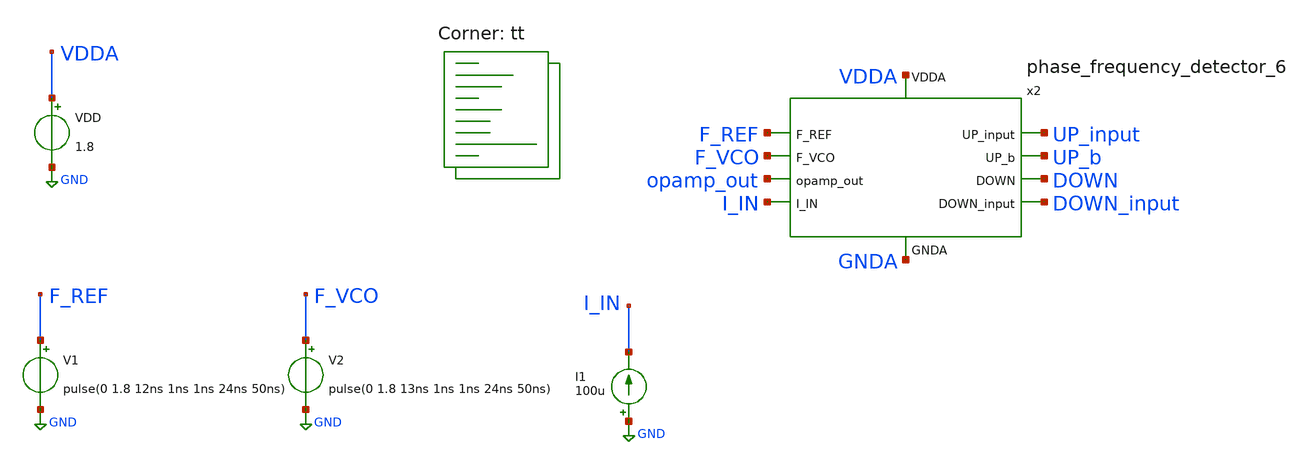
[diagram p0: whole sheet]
** sch_path: projects/pll/pfd/xschem_ngspice/tb_phase_frequency_detector_3.sch
**.subckt tb_phase_frequency_detector_3
V1 F_REF GND pulse(0 1.8 12ns 1ns 1ns 24ns 50ns)
V2 F_VCO GND pulse(0 1.8 13ns 1ns 1ns 24ns 50ns)
VDD VDDA GND 1.8
x2 UP_input VDDA GNDA UP_b F_REF DOWN F_VCO DOWN_input opamp_out I_IN phase_frequency_detector_6
I1 GND I_IN 100u
**** begin user architecture code
.lib $::SKYWATER_MODELS/sky130.lib.spice tt



.option wnflag=1
.option method=gear trtol=1

.save v(x1.reset)
.save v(x1.qb_b)
.save v(x1.qa_b)
.save v(x1.f_b)
.save v(x1.f)
.save v(x1.e_b)
.save v(x1.e)
.save v(x1.before_reset)
.save v(qb)
.save v(qa)
.save v(f_vco)
.save v(f_ref)
.save v(f_vco)

.control

  tran 1ns 1us
  remzerovec
  write tb_phase_frequency_detector_3.raw
  set appendwrite

.endc



**** end user architecture code
**.ends

* expanding   symbol:  phase_frequency_detector_6.sym # of pins=10
** sym_path: projects/pll/pfd/xschem_ngspice/phase_frequency_detector_6.sym
** sch_path: projects/pll/pfd/xschem_ngspice/phase_frequency_detector_6.sch
.subckt phase_frequency_detector_6 UP_input VDDA GNDA UP_b F_REF DOWN F_VCO DOWN_input opamp_out
+ I_IN
*.ipin F_REF
*.ipin F_VCO
*.ipin VDDA
*.ipin GNDA
*.opin UP_input
*.opin DOWN_input
*.opin UP_b
*.opin DOWN
*.ipin opamp_out
*.ipin I_IN
XM1 DOWN_b GNDA DOWN_PFD_b VDDA sky130_fd_pr__pfet_01v8 L=0.15 W=2 nf=2 ad='int((nf+1)/2) * W/nf * 0.29'
+ as='int((nf+2)/2) * W/nf * 0.29' pd='2*int((nf+1)/2) * (W/nf + 0.29)' ps='2*int((nf+2)/2) * (W/nf + 0.29)'
+ nrd='0.29 / W' nrs='0.29 / W' sa=0 sb=0 sd=0 mult=1 m=1
XM2 DOWN_b VDDA DOWN_PFD_b GNDA sky130_fd_pr__nfet_01v8 L=0.15 W=1 nf=1 ad='int((nf+1)/2) * W/nf * 0.29'
+ as='int((nf+2)/2) * W/nf * 0.29' pd='2*int((nf+1)/2) * (W/nf + 0.29)' ps='2*int((nf+2)/2) * (W/nf + 0.29)'
+ nrd='0.29 / W' nrs='0.29 / W' sa=0 sb=0 sd=0 mult=1 m=1
XM3 DOWN_PFD_b QB VDDA VDDA sky130_fd_pr__pfet_01v8 L=0.15 W=2 nf=2 ad='int((nf+1)/2) * W/nf * 0.29'
+ as='int((nf+2)/2) * W/nf * 0.29' pd='2*int((nf+1)/2) * (W/nf + 0.29)' ps='2*int((nf+2)/2) * (W/nf + 0.29)'
+ nrd='0.29 / W' nrs='0.29 / W' sa=0 sb=0 sd=0 mult=1 m=1
XM4 GNDA QB DOWN_PFD_b GNDA sky130_fd_pr__nfet_01v8 L=0.15 W=1 nf=1 ad='int((nf+1)/2) * W/nf * 0.29'
+ as='int((nf+2)/2) * W/nf * 0.29' pd='2*int((nf+1)/2) * (W/nf + 0.29)' ps='2*int((nf+2)/2) * (W/nf + 0.29)'
+ nrd='0.29 / W' nrs='0.29 / W' sa=0 sb=0 sd=0 mult=1 m=1
XM5 UP_PFD_b QA VDDA VDDA sky130_fd_pr__pfet_01v8 L=0.15 W=2 nf=2 ad='int((nf+1)/2) * W/nf * 0.29' as='int((nf+2)/2) * W/nf * 0.29'
+ pd='2*int((nf+1)/2) * (W/nf + 0.29)' ps='2*int((nf+2)/2) * (W/nf + 0.29)' nrd='0.29 / W' nrs='0.29 / W'
+ sa=0 sb=0 sd=0 mult=1 m=1
XM6 GNDA QA UP_PFD_b GNDA sky130_fd_pr__nfet_01v8 L=0.15 W=1 nf=1 ad='int((nf+1)/2) * W/nf * 0.29' as='int((nf+2)/2) * W/nf * 0.29'
+ pd='2*int((nf+1)/2) * (W/nf + 0.29)' ps='2*int((nf+2)/2) * (W/nf + 0.29)' nrd='0.29 / W' nrs='0.29 / W'
+ sa=0 sb=0 sd=0 mult=1 m=1
XM7 UP UP_PFD_b VDDA VDDA sky130_fd_pr__pfet_01v8 L=0.15 W=2 nf=2 ad='int((nf+1)/2) * W/nf * 0.29' as='int((nf+2)/2) * W/nf * 0.29'
+ pd='2*int((nf+1)/2) * (W/nf + 0.29)' ps='2*int((nf+2)/2) * (W/nf + 0.29)' nrd='0.29 / W' nrs='0.29 / W'
+ sa=0 sb=0 sd=0 mult=1 m=1
XM8 GNDA UP_PFD_b UP GNDA sky130_fd_pr__nfet_01v8 L=0.15 W=1 nf=1 ad='int((nf+1)/2) * W/nf * 0.29' as='int((nf+2)/2) * W/nf * 0.29'
+ pd='2*int((nf+1)/2) * (W/nf + 0.29)' ps='2*int((nf+2)/2) * (W/nf + 0.29)' nrd='0.29 / W' nrs='0.29 / W'
+ sa=0 sb=0 sd=0 mult=1 m=1
XM9 UP_input UP_b opamp_out VDDA sky130_fd_pr__pfet_01v8 L=0.15 W=2 nf=2 ad='int((nf+1)/2) * W/nf * 0.29'
+ as='int((nf+2)/2) * W/nf * 0.29' pd='2*int((nf+1)/2) * (W/nf + 0.29)' ps='2*int((nf+2)/2) * (W/nf + 0.29)'
+ nrd='0.29 / W' nrs='0.29 / W' sa=0 sb=0 sd=0 mult=1 m=1
XM18 UP_input UP VDDA VDDA sky130_fd_pr__pfet_01v8 L=0.15 W=2 nf=2 ad='int((nf+1)/2) * W/nf * 0.29' as='int((nf+2)/2) * W/nf * 0.29'
+ pd='2*int((nf+1)/2) * (W/nf + 0.29)' ps='2*int((nf+2)/2) * (W/nf + 0.29)' nrd='0.29 / W' nrs='0.29 / W'
+ sa=0 sb=0 sd=0 mult=1 m=1
XM19 DOWN_input DOWN I_IN GNDA sky130_fd_pr__nfet_01v8 L=0.15 W=1 nf=1 ad='int((nf+1)/2) * W/nf * 0.29'
+ as='int((nf+2)/2) * W/nf * 0.29' pd='2*int((nf+1)/2) * (W/nf + 0.29)' ps='2*int((nf+2)/2) * (W/nf + 0.29)'
+ nrd='0.29 / W' nrs='0.29 / W' sa=0 sb=0 sd=0 mult=1 m=1
XM20 DOWN_input DOWN_b GNDA GNDA sky130_fd_pr__nfet_01v8 L=0.15 W=1 nf=1 ad='int((nf+1)/2) * W/nf * 0.29'
+ as='int((nf+2)/2) * W/nf * 0.29' pd='2*int((nf+1)/2) * (W/nf + 0.29)' ps='2*int((nf+2)/2) * (W/nf + 0.29)'
+ nrd='0.29 / W' nrs='0.29 / W' sa=0 sb=0 sd=0 mult=1 m=1
XM21 DOWN DOWN_b VDDA VDDA sky130_fd_pr__pfet_01v8 L=0.15 W=2 nf=2 ad='int((nf+1)/2) * W/nf * 0.29' as='int((nf+2)/2) * W/nf * 0.29'
+ pd='2*int((nf+1)/2) * (W/nf + 0.29)' ps='2*int((nf+2)/2) * (W/nf + 0.29)' nrd='0.29 / W' nrs='0.29 / W'
+ sa=0 sb=0 sd=0 mult=1 m=1
XM22 GNDA DOWN_b DOWN GNDA sky130_fd_pr__nfet_01v8 L=0.15 W=1 nf=1 ad='int((nf+1)/2) * W/nf * 0.29' as='int((nf+2)/2) * W/nf * 0.29'
+ pd='2*int((nf+1)/2) * (W/nf + 0.29)' ps='2*int((nf+2)/2) * (W/nf + 0.29)' nrd='0.29 / W' nrs='0.29 / W'
+ sa=0 sb=0 sd=0 mult=1 m=1
XM23 UP_b UP VDDA VDDA sky130_fd_pr__pfet_01v8 L=0.15 W=2 nf=2 ad='int((nf+1)/2) * W/nf * 0.29' as='int((nf+2)/2) * W/nf * 0.29'
+ pd='2*int((nf+1)/2) * (W/nf + 0.29)' ps='2*int((nf+2)/2) * (W/nf + 0.29)' nrd='0.29 / W' nrs='0.29 / W'
+ sa=0 sb=0 sd=0 mult=1 m=1
XM24 GNDA UP UP_b GNDA sky130_fd_pr__nfet_01v8 L=0.15 W=1 nf=1 ad='int((nf+1)/2) * W/nf * 0.29' as='int((nf+2)/2) * W/nf * 0.29'
+ pd='2*int((nf+1)/2) * (W/nf + 0.29)' ps='2*int((nf+2)/2) * (W/nf + 0.29)' nrd='0.29 / W' nrs='0.29 / W'
+ sa=0 sb=0 sd=0 mult=1 m=1
XM27 UP_input UP opamp_out GNDA sky130_fd_pr__nfet_01v8 L=0.15 W=1 nf=1 ad='int((nf+1)/2) * W/nf * 0.29'
+ as='int((nf+2)/2) * W/nf * 0.29' pd='2*int((nf+1)/2) * (W/nf + 0.29)' ps='2*int((nf+2)/2) * (W/nf + 0.29)'
+ nrd='0.29 / W' nrs='0.29 / W' sa=0 sb=0 sd=0 mult=1 m=1
XM30 DOWN_input DOWN_b I_IN VDDA sky130_fd_pr__pfet_01v8 L=0.15 W=2 nf=2 ad='int((nf+1)/2) * W/nf * 0.29'
+ as='int((nf+2)/2) * W/nf * 0.29' pd='2*int((nf+1)/2) * (W/nf + 0.29)' ps='2*int((nf+2)/2) * (W/nf + 0.29)'
+ nrd='0.29 / W' nrs='0.29 / W' sa=0 sb=0 sd=0 mult=1 m=1
x15 VDDA GNDA QA F_REF QA_b nor_pfd
x16 VDDA GNDA QB F_VCO QB_b nor_pfd
x17 VDDA GNDA QA_b E QA nor_pfd
x18 VDDA GNDA QB_b F QB nor_pfd
x19 VDDA GNDA E_b QA_b E nor_pfd
x20 VDDA GNDA F_b QB_b F nor_pfd
x21 VDDA GNDA E Reset E_b nor_pfd
x22 VDDA GNDA F Reset F_b nor_pfd
x23 VDDA GNDA QB QA before_Reset nand_pfd
x24 VDDA GNDA before_Reset net1 inv_pfd
x25 VDDA GNDA net1 net2 inv_pfd
x26 VDDA GNDA net2 net3 inv_pfd
x27 VDDA GNDA net3 net4 inv_pfd
x28 VDDA GNDA net4 Reset inv_pfd
.ends


* expanding   symbol:  /foss/designs/my_design/projects/pll/pfd/xschem_ngspice/nor_pfd.sym # of
*+ pins=5
** sym_path: projects/pll/pfd/xschem_ngspice/nor_pfd.sym
** sch_path: projects/pll/pfd/xschem_ngspice/nor_pfd.sch
.subckt nor_pfd VDDA GNDA A B Y
*.ipin A
*.opin Y
*.ipin VDDA
*.ipin GNDA
*.ipin B
XM4 net1 B VDDA VDDA sky130_fd_pr__pfet_01v8 L=0.15 W=2 nf=1 ad='int((nf+1)/2) * W/nf * 0.29' as='int((nf+2)/2) * W/nf * 0.29'
+ pd='2*int((nf+1)/2) * (W/nf + 0.29)' ps='2*int((nf+2)/2) * (W/nf + 0.29)' nrd='0.29 / W' nrs='0.29 / W'
+ sa=0 sb=0 sd=0 mult=1 m=1
XM2 GNDA B Y GNDA sky130_fd_pr__nfet_01v8 L=0.15 W=1 nf=1 ad='int((nf+1)/2) * W/nf * 0.29' as='int((nf+2)/2) * W/nf * 0.29'
+ pd='2*int((nf+1)/2) * (W/nf + 0.29)' ps='2*int((nf+2)/2) * (W/nf + 0.29)' nrd='0.29 / W' nrs='0.29 / W'
+ sa=0 sb=0 sd=0 mult=1 m=1
XM1 GNDA A Y GNDA sky130_fd_pr__nfet_01v8 L=0.15 W=1 nf=1 ad='int((nf+1)/2) * W/nf * 0.29' as='int((nf+2)/2) * W/nf * 0.29'
+ pd='2*int((nf+1)/2) * (W/nf + 0.29)' ps='2*int((nf+2)/2) * (W/nf + 0.29)' nrd='0.29 / W' nrs='0.29 / W'
+ sa=0 sb=0 sd=0 mult=1 m=1
XM3 Y A net1 VDDA sky130_fd_pr__pfet_01v8 L=0.15 W=2 nf=1 ad='int((nf+1)/2) * W/nf * 0.29' as='int((nf+2)/2) * W/nf * 0.29'
+ pd='2*int((nf+1)/2) * (W/nf + 0.29)' ps='2*int((nf+2)/2) * (W/nf + 0.29)' nrd='0.29 / W' nrs='0.29 / W'
+ sa=0 sb=0 sd=0 mult=1 m=1
.ends


* expanding   symbol:  /foss/designs/my_design/projects/pll/pfd/xschem_ngspice/nand_pfd.sym # of
*+ pins=5
** sym_path: projects/pll/pfd/xschem_ngspice/nand_pfd.sym
** sch_path: projects/pll/pfd/xschem_ngspice/nand_pfd.sch
.subckt nand_pfd VDDA GNDA A B Y
*.ipin A
*.opin Y
*.ipin VDDA
*.ipin GNDA
*.ipin B
XM4 Y B VDDA VDDA sky130_fd_pr__pfet_01v8 L=0.15 W=1 nf=2 ad='int((nf+1)/2) * W/nf * 0.29' as='int((nf+2)/2) * W/nf * 0.29'
+ pd='2*int((nf+1)/2) * (W/nf + 0.29)' ps='2*int((nf+2)/2) * (W/nf + 0.29)' nrd='0.29 / W' nrs='0.29 / W'
+ sa=0 sb=0 sd=0 mult=1 m=1
XM2 net1 B Y GNDA sky130_fd_pr__nfet_01v8 L=0.15 W=0.5 nf=1 ad='int((nf+1)/2) * W/nf * 0.29' as='int((nf+2)/2) * W/nf * 0.29'
+ pd='2*int((nf+1)/2) * (W/nf + 0.29)' ps='2*int((nf+2)/2) * (W/nf + 0.29)' nrd='0.29 / W' nrs='0.29 / W'
+ sa=0 sb=0 sd=0 mult=1 m=1
XM1 GNDA A net1 GNDA sky130_fd_pr__nfet_01v8 L=0.15 W=0.5 nf=1 ad='int((nf+1)/2) * W/nf * 0.29' as='int((nf+2)/2) * W/nf * 0.29'
+ pd='2*int((nf+1)/2) * (W/nf + 0.29)' ps='2*int((nf+2)/2) * (W/nf + 0.29)' nrd='0.29 / W' nrs='0.29 / W'
+ sa=0 sb=0 sd=0 mult=1 m=1
XM3 Y A VDDA VDDA sky130_fd_pr__pfet_01v8 L=0.15 W=1 nf=2 ad='int((nf+1)/2) * W/nf * 0.29' as='int((nf+2)/2) * W/nf * 0.29'
+ pd='2*int((nf+1)/2) * (W/nf + 0.29)' ps='2*int((nf+2)/2) * (W/nf + 0.29)' nrd='0.29 / W' nrs='0.29 / W'
+ sa=0 sb=0 sd=0 mult=1 m=1
.ends


* expanding   symbol:  /foss/designs/my_design/projects/pll/pfd/xschem_ngspice/inv_pfd.sym # of
*+ pins=4
** sym_path: projects/ASU/EEE572/schematic/inv_pfd.sym
** sch_path: projects/ASU/EEE572/schematic/inv_pfd.sch
.subckt inv_pfd VDDA GNDA A Y
*.ipin A
*.opin Y
*.ipin VDDA
*.ipin GNDA
XM2 Y A VDDA VDDA sky130_fd_pr__pfet_01v8 L=0.15 W=2 nf=1 ad='int((nf+1)/2) * W/nf * 0.29' as='int((nf+2)/2) * W/nf * 0.29'
+ pd='2*int((nf+1)/2) * (W/nf + 0.29)' ps='2*int((nf+2)/2) * (W/nf + 0.29)' nrd='0.29 / W' nrs='0.29 / W'
+ sa=0 sb=0 sd=0 mult=1 m=1
XM1 GNDA A Y GNDA sky130_fd_pr__nfet_01v8 L=0.15 W=1 nf=1 ad='int((nf+1)/2) * W/nf * 0.29' as='int((nf+2)/2) * W/nf * 0.29'
+ pd='2*int((nf+1)/2) * (W/nf + 0.29)' ps='2*int((nf+2)/2) * (W/nf + 0.29)' nrd='0.29 / W' nrs='0.29 / W'
+ sa=0 sb=0 sd=0 mult=1 m=1
.ends

.GLOBAL GND
.end
